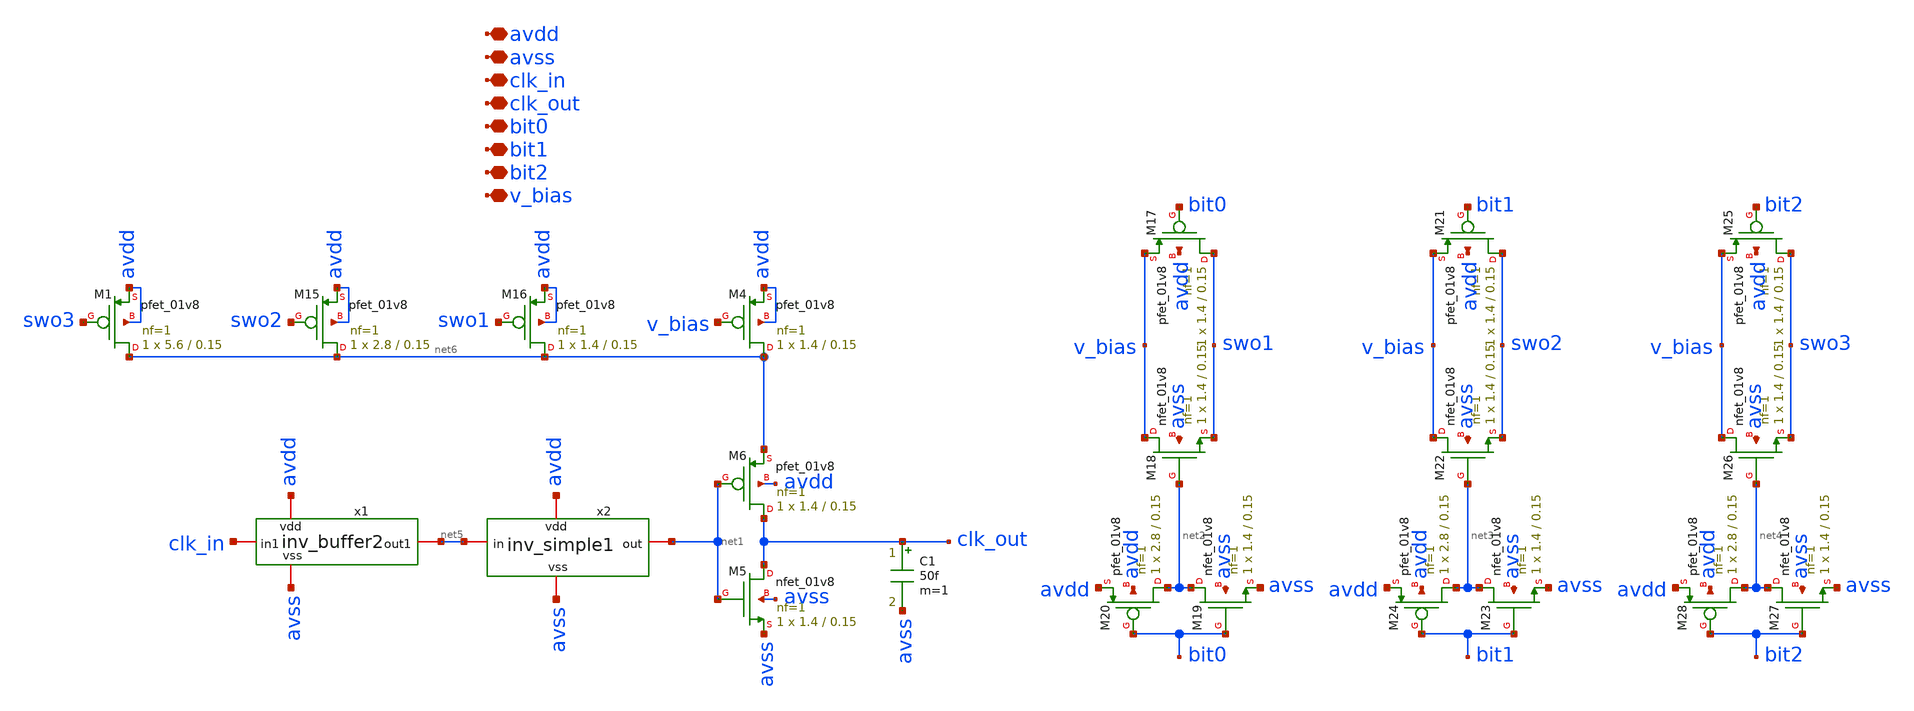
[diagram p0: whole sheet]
** sch_path: xschem/slopebuf.sch
**.subckt slopebuf avdd avss clk_in clk_out bit0 bit1 bit2 v_bias
*.iopin avdd
*.iopin avss
*.iopin clk_in
*.iopin clk_out
*.iopin bit0
*.iopin bit1
*.iopin bit2
*.iopin v_bias
XM5 clk_out net1 avss avss sky130_fd_pr__nfet_01v8 L=0.15 W=1.4 nf=1 ad='int((nf+1)/2) * W/nf * 0.29'
+ as='int((nf+2)/2) * W/nf * 0.29' pd='2*int((nf+1)/2) * (W/nf + 0.29)' ps='2*int((nf+2)/2) * (W/nf + 0.29)'
+ nrd='0.29 / W' nrs='0.29 / W' sa=0 sb=0 sd=0 mult=1 m=1
XM6 clk_out net1 net6 avdd sky130_fd_pr__pfet_01v8 L=0.15 W=1.4 nf=1 ad='int((nf+1)/2) * W/nf * 0.29'
+ as='int((nf+2)/2) * W/nf * 0.29' pd='2*int((nf+1)/2) * (W/nf + 0.29)' ps='2*int((nf+2)/2) * (W/nf + 0.29)'
+ nrd='0.29 / W' nrs='0.29 / W' sa=0 sb=0 sd=0 mult=1 m=1
XM4 net6 v_bias avdd avdd sky130_fd_pr__pfet_01v8 L=0.15 W=1.4 nf=1 ad='int((nf+1)/2) * W/nf * 0.29'
+ as='int((nf+2)/2) * W/nf * 0.29' pd='2*int((nf+1)/2) * (W/nf + 0.29)' ps='2*int((nf+2)/2) * (W/nf + 0.29)'
+ nrd='0.29 / W' nrs='0.29 / W' sa=0 sb=0 sd=0 mult=1 m=1
C1 clk_out avss 50f m=1
XM1 net6 swo3 avdd avdd sky130_fd_pr__pfet_01v8 L=0.15 W=5.6 nf=1 ad='int((nf+1)/2) * W/nf * 0.29' as='int((nf+2)/2) * W/nf * 0.29'
+ pd='2*int((nf+1)/2) * (W/nf + 0.29)' ps='2*int((nf+2)/2) * (W/nf + 0.29)' nrd='0.29 / W' nrs='0.29 / W'
+ sa=0 sb=0 sd=0 mult=1 m=1
XM15 net6 swo2 avdd avdd sky130_fd_pr__pfet_01v8 L=0.15 W=2.8 nf=1 ad='int((nf+1)/2) * W/nf * 0.29' as='int((nf+2)/2) * W/nf * 0.29'
+ pd='2*int((nf+1)/2) * (W/nf + 0.29)' ps='2*int((nf+2)/2) * (W/nf + 0.29)' nrd='0.29 / W' nrs='0.29 / W'
+ sa=0 sb=0 sd=0 mult=1 m=1
XM16 net6 swo1 avdd avdd sky130_fd_pr__pfet_01v8 L=0.15 W=1.4 nf=1 ad='int((nf+1)/2) * W/nf * 0.29' as='int((nf+2)/2) * W/nf * 0.29'
+ pd='2*int((nf+1)/2) * (W/nf + 0.29)' ps='2*int((nf+2)/2) * (W/nf + 0.29)' nrd='0.29 / W' nrs='0.29 / W'
+ sa=0 sb=0 sd=0 mult=1 m=1
XM17 swo1 bit0 v_bias avdd sky130_fd_pr__pfet_01v8 L=0.15 W=1.4 nf=1 ad='int((nf+1)/2) * W/nf * 0.29'
+ as='int((nf+2)/2) * W/nf * 0.29' pd='2*int((nf+1)/2) * (W/nf + 0.29)' ps='2*int((nf+2)/2) * (W/nf + 0.29)'
+ nrd='0.29 / W' nrs='0.29 / W' sa=0 sb=0 sd=0 mult=1 m=1
XM18 v_bias net2 swo1 avss sky130_fd_pr__nfet_01v8 L=0.15 W=1.4 nf=1 ad='int((nf+1)/2) * W/nf * 0.29'
+ as='int((nf+2)/2) * W/nf * 0.29' pd='2*int((nf+1)/2) * (W/nf + 0.29)' ps='2*int((nf+2)/2) * (W/nf + 0.29)'
+ nrd='0.29 / W' nrs='0.29 / W' sa=0 sb=0 sd=0 mult=1 m=1
XM19 net2 bit0 avss avss sky130_fd_pr__nfet_01v8 L=0.15 W=1.4 nf=1 ad='int((nf+1)/2) * W/nf * 0.29' as='int((nf+2)/2) * W/nf * 0.29'
+ pd='2*int((nf+1)/2) * (W/nf + 0.29)' ps='2*int((nf+2)/2) * (W/nf + 0.29)' nrd='0.29 / W' nrs='0.29 / W'
+ sa=0 sb=0 sd=0 mult=1 m=1
XM20 net2 bit0 avdd avdd sky130_fd_pr__pfet_01v8 L=0.15 W=2.8 nf=1 ad='int((nf+1)/2) * W/nf * 0.29' as='int((nf+2)/2) * W/nf * 0.29'
+ pd='2*int((nf+1)/2) * (W/nf + 0.29)' ps='2*int((nf+2)/2) * (W/nf + 0.29)' nrd='0.29 / W' nrs='0.29 / W'
+ sa=0 sb=0 sd=0 mult=1 m=1
XM21 swo2 bit1 v_bias avdd sky130_fd_pr__pfet_01v8 L=0.15 W=1.4 nf=1 ad='int((nf+1)/2) * W/nf * 0.29'
+ as='int((nf+2)/2) * W/nf * 0.29' pd='2*int((nf+1)/2) * (W/nf + 0.29)' ps='2*int((nf+2)/2) * (W/nf + 0.29)'
+ nrd='0.29 / W' nrs='0.29 / W' sa=0 sb=0 sd=0 mult=1 m=1
XM22 v_bias net3 swo2 avss sky130_fd_pr__nfet_01v8 L=0.15 W=1.4 nf=1 ad='int((nf+1)/2) * W/nf * 0.29'
+ as='int((nf+2)/2) * W/nf * 0.29' pd='2*int((nf+1)/2) * (W/nf + 0.29)' ps='2*int((nf+2)/2) * (W/nf + 0.29)'
+ nrd='0.29 / W' nrs='0.29 / W' sa=0 sb=0 sd=0 mult=1 m=1
XM23 net3 bit1 avss avss sky130_fd_pr__nfet_01v8 L=0.15 W=1.4 nf=1 ad='int((nf+1)/2) * W/nf * 0.29' as='int((nf+2)/2) * W/nf * 0.29'
+ pd='2*int((nf+1)/2) * (W/nf + 0.29)' ps='2*int((nf+2)/2) * (W/nf + 0.29)' nrd='0.29 / W' nrs='0.29 / W'
+ sa=0 sb=0 sd=0 mult=1 m=1
XM24 net3 bit1 avdd avdd sky130_fd_pr__pfet_01v8 L=0.15 W=2.8 nf=1 ad='int((nf+1)/2) * W/nf * 0.29' as='int((nf+2)/2) * W/nf * 0.29'
+ pd='2*int((nf+1)/2) * (W/nf + 0.29)' ps='2*int((nf+2)/2) * (W/nf + 0.29)' nrd='0.29 / W' nrs='0.29 / W'
+ sa=0 sb=0 sd=0 mult=1 m=1
XM25 swo3 bit2 v_bias avdd sky130_fd_pr__pfet_01v8 L=0.15 W=1.4 nf=1 ad='int((nf+1)/2) * W/nf * 0.29'
+ as='int((nf+2)/2) * W/nf * 0.29' pd='2*int((nf+1)/2) * (W/nf + 0.29)' ps='2*int((nf+2)/2) * (W/nf + 0.29)'
+ nrd='0.29 / W' nrs='0.29 / W' sa=0 sb=0 sd=0 mult=1 m=1
XM26 v_bias net4 swo3 avss sky130_fd_pr__nfet_01v8 L=0.15 W=1.4 nf=1 ad='int((nf+1)/2) * W/nf * 0.29'
+ as='int((nf+2)/2) * W/nf * 0.29' pd='2*int((nf+1)/2) * (W/nf + 0.29)' ps='2*int((nf+2)/2) * (W/nf + 0.29)'
+ nrd='0.29 / W' nrs='0.29 / W' sa=0 sb=0 sd=0 mult=1 m=1
XM27 net4 bit2 avss avss sky130_fd_pr__nfet_01v8 L=0.15 W=1.4 nf=1 ad='int((nf+1)/2) * W/nf * 0.29' as='int((nf+2)/2) * W/nf * 0.29'
+ pd='2*int((nf+1)/2) * (W/nf + 0.29)' ps='2*int((nf+2)/2) * (W/nf + 0.29)' nrd='0.29 / W' nrs='0.29 / W'
+ sa=0 sb=0 sd=0 mult=1 m=1
XM28 net4 bit2 avdd avdd sky130_fd_pr__pfet_01v8 L=0.15 W=2.8 nf=1 ad='int((nf+1)/2) * W/nf * 0.29' as='int((nf+2)/2) * W/nf * 0.29'
+ pd='2*int((nf+1)/2) * (W/nf + 0.29)' ps='2*int((nf+2)/2) * (W/nf + 0.29)' nrd='0.29 / W' nrs='0.29 / W'
+ sa=0 sb=0 sd=0 mult=1 m=1
x2 avdd net5 net1 avss inv_simple1
x1 avdd avss net5 clk_in inv_buffer2
**.ends

* expanding   symbol:  ma2022/inv_simple1.sym # of pins=4
** sym_path: xschem/inv_simple1.sym
** sch_path: xschem/inv_simple1.sch
.subckt inv_simple1 vdd in out vss
*.iopin in
*.iopin vdd
*.iopin vss
*.iopin out
XM19 out in vss vss sky130_fd_pr__nfet_01v8 L=0.15 W=1.4 nf=1 ad='int((nf+1)/2) * W/nf * 0.29' as='int((nf+2)/2) * W/nf * 0.29'
+ pd='2*int((nf+1)/2) * (W/nf + 0.29)' ps='2*int((nf+2)/2) * (W/nf + 0.29)' nrd='0.29 / W' nrs='0.29 / W'
+ sa=0 sb=0 sd=0 mult=1 m=1
XM20 out in vdd vdd sky130_fd_pr__pfet_01v8 L=0.15 W=2.8 nf=1 ad='int((nf+1)/2) * W/nf * 0.29' as='int((nf+2)/2) * W/nf * 0.29'
+ pd='2*int((nf+1)/2) * (W/nf + 0.29)' ps='2*int((nf+2)/2) * (W/nf + 0.29)' nrd='0.29 / W' nrs='0.29 / W'
+ sa=0 sb=0 sd=0 mult=1 m=1
XM1 vdd vdd vdd vdd sky130_fd_pr__pfet_01v8 L=0.15 W=1.4 nf=1 ad='int((nf+1)/2) * W/nf * 0.29' as='int((nf+2)/2) * W/nf * 0.29'
+ pd='2*int((nf+1)/2) * (W/nf + 0.29)' ps='2*int((nf+2)/2) * (W/nf + 0.29)' nrd='0.29 / W' nrs='0.29 / W'
+ sa=0 sb=0 sd=0 mult=1 m=1
XM2 vss vss vss vss sky130_fd_pr__nfet_01v8 L=0.15 W=1.4 nf=1 ad='int((nf+1)/2) * W/nf * 0.29' as='int((nf+2)/2) * W/nf * 0.29'
+ pd='2*int((nf+1)/2) * (W/nf + 0.29)' ps='2*int((nf+2)/2) * (W/nf + 0.29)' nrd='0.29 / W' nrs='0.29 / W'
+ sa=0 sb=0 sd=0 mult=1 m=1
.ends


* expanding   symbol:  ma2022/inv_buffer2.sym # of pins=4
** sym_path: xschem/inv_buffer2.sym
** sch_path: xschem/inv_buffer2.sch
.subckt inv_buffer2 vdd vss out1 in1
*.iopin in1
*.iopin out1
*.iopin vdd
*.iopin vss
XM4 out1 net1 vss vss sky130_fd_pr__nfet_01v8 L=0.15 W=2.8 nf=4 ad='int((nf+1)/2) * W/nf * 0.29' as='int((nf+2)/2) * W/nf * 0.29'
+ pd='2*int((nf+1)/2) * (W/nf + 0.29)' ps='2*int((nf+2)/2) * (W/nf + 0.29)' nrd='0.29 / W' nrs='0.29 / W'
+ sa=0 sb=0 sd=0 mult=1 m=1
XM1 out1 net1 vdd vdd sky130_fd_pr__pfet_01v8 L=0.15 W=5.6 nf=8 ad='int((nf+1)/2) * W/nf * 0.29' as='int((nf+2)/2) * W/nf * 0.29'
+ pd='2*int((nf+1)/2) * (W/nf + 0.29)' ps='2*int((nf+2)/2) * (W/nf + 0.29)' nrd='0.29 / W' nrs='0.29 / W'
+ sa=0 sb=0 sd=0 mult=1 m=1
XM5 vdd vdd vdd vdd sky130_fd_pr__pfet_01v8 L=0.15 W=1.4 nf=2 ad='int((nf+1)/2) * W/nf * 0.29' as='int((nf+2)/2) * W/nf * 0.29'
+ pd='2*int((nf+1)/2) * (W/nf + 0.29)' ps='2*int((nf+2)/2) * (W/nf + 0.29)' nrd='0.29 / W' nrs='0.29 / W'
+ sa=0 sb=0 sd=0 mult=1 m=1
XM6 vss vss vss vss sky130_fd_pr__nfet_01v8 L=0.15 W=1.4 nf=2 ad='int((nf+1)/2) * W/nf * 0.29' as='int((nf+2)/2) * W/nf * 0.29'
+ pd='2*int((nf+1)/2) * (W/nf + 0.29)' ps='2*int((nf+2)/2) * (W/nf + 0.29)' nrd='0.29 / W' nrs='0.29 / W'
+ sa=0 sb=0 sd=0 mult=1 m=1
x1 vdd in1 net1 vss inv_simple1
.ends

.end
